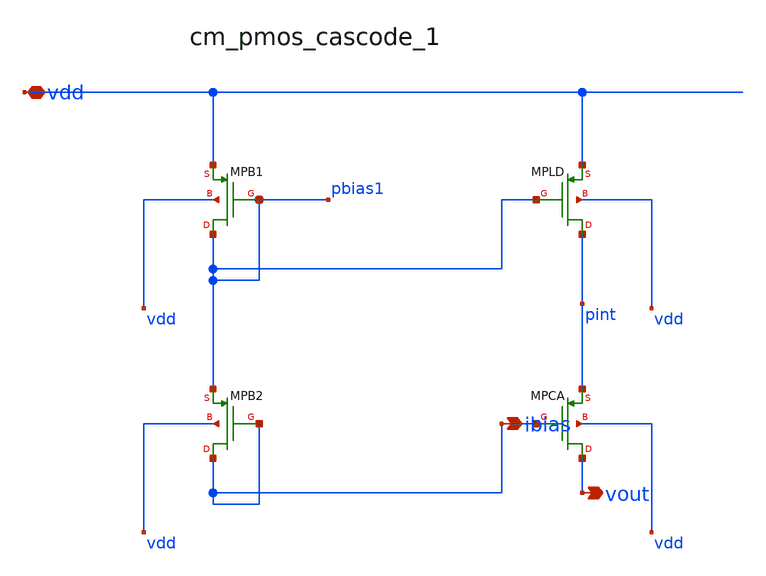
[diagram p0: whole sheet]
** sch_path: analog-db/raw/gs_001_cascode_cs/hier/blocks/cm_pmos_cascode_1.sch
**.subckt cm_pmos_cascode_1 vdd ibias vout
*.iopin vdd
*.opin ibias
*.opin vout
XMPB1 pbias1 pbias1 vdd vdd sg13_lv_pmos w=x_dut_xmpb1_w l=x_dut_xmpb1_l ng=1 m=x_dut_xmpb1_m
XMPB2 ibias ibias pbias1 vdd sg13_lv_pmos w=x_dut_xmpb2_w l=x_dut_xmpb2_l ng=1 m=x_dut_xmpb2_m
XMPCA vout ibias pint vdd sg13_lv_pmos w=x_dut_xmpca_w l=x_dut_xmpca_l ng=1 m=x_dut_xmpca_m
XMPLD pint pbias1 vdd vdd sg13_lv_pmos w=x_dut_xmpld_w l=x_dut_xmpld_l ng=1 m=x_dut_xmpld_m
**.ends
.end
